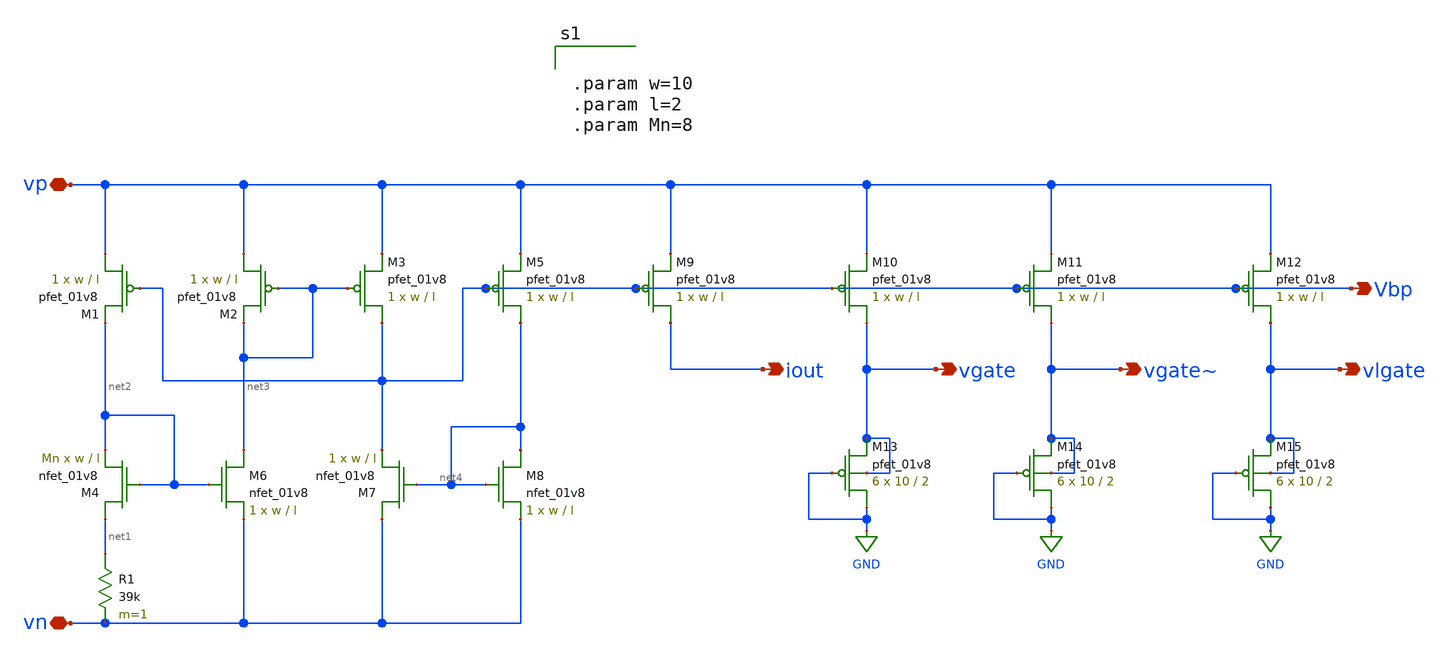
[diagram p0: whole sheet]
** sch_path: schematic/bias_current_resistive.sch
**.subckt bias_current_resistive vp vn iout vgate vgate~ Vbp vlgate
*.iopin vp
*.iopin vn
*.opin iout
*.opin vgate
*.opin vgate~
*.opin Vbp
*.opin vlgate
XM1 vp Vbp net2 VDD sky130_fd_pr__pfet_01v8 L=l W=w nf=1 ad='int((nf+1)/2) * W/nf * 0.29' as='int((nf+2)/2) * W/nf * 0.29'
+ pd='2*int((nf+1)/2) * (W/nf + 0.29)' ps='2*int((nf+2)/2) * (W/nf + 0.29)' nrd='0.29 / W' nrs='0.29 / W'
+ sa=0 sb=0 sd=0 mult=1 m=1
XM2 vp net3 net3 VDD sky130_fd_pr__pfet_01v8 L=l W=w nf=1 ad='int((nf+1)/2) * W/nf * 0.29' as='int((nf+2)/2) * W/nf * 0.29'
+ pd='2*int((nf+1)/2) * (W/nf + 0.29)' ps='2*int((nf+2)/2) * (W/nf + 0.29)' nrd='0.29 / W' nrs='0.29 / W'
+ sa=0 sb=0 sd=0 mult=1 m=1
XM3 Vbp net3 vp VDD sky130_fd_pr__pfet_01v8 L=l W=w nf=1 ad='int((nf+1)/2) * W/nf * 0.29' as='int((nf+2)/2) * W/nf * 0.29'
+ pd='2*int((nf+1)/2) * (W/nf + 0.29)' ps='2*int((nf+2)/2) * (W/nf + 0.29)' nrd='0.29 / W' nrs='0.29 / W'
+ sa=0 sb=0 sd=0 mult=1 m=1
XM5 net4 Vbp vp VDD sky130_fd_pr__pfet_01v8 L=l W=w nf=1 ad='int((nf+1)/2) * W/nf * 0.29' as='int((nf+2)/2) * W/nf * 0.29'
+ pd='2*int((nf+1)/2) * (W/nf + 0.29)' ps='2*int((nf+2)/2) * (W/nf + 0.29)' nrd='0.29 / W' nrs='0.29 / W'
+ sa=0 sb=0 sd=0 mult=1 m=1
XM4 net1 net2 net2 GND sky130_fd_pr__nfet_01v8 L=l W=w nf=1 ad='int((nf+1)/2) * W/nf * 0.29' as='int((nf+2)/2) * W/nf * 0.29'
+ pd='2*int((nf+1)/2) * (W/nf + 0.29)' ps='2*int((nf+2)/2) * (W/nf + 0.29)' nrd='0.29 / W' nrs='0.29 / W'
+ sa=0 sb=0 sd=0 mult=Mn m=Mn
XM6 net3 net2 vn GND sky130_fd_pr__nfet_01v8 L=l W=w nf=1 ad='int((nf+1)/2) * W/nf * 0.29' as='int((nf+2)/2) * W/nf * 0.29'
+ pd='2*int((nf+1)/2) * (W/nf + 0.29)' ps='2*int((nf+2)/2) * (W/nf + 0.29)' nrd='0.29 / W' nrs='0.29 / W'
+ sa=0 sb=0 sd=0 mult=1 m=1
XM7 vn net4 Vbp GND sky130_fd_pr__nfet_01v8 L=l W=w nf=1 ad='int((nf+1)/2) * W/nf * 0.29' as='int((nf+2)/2) * W/nf * 0.29'
+ pd='2*int((nf+1)/2) * (W/nf + 0.29)' ps='2*int((nf+2)/2) * (W/nf + 0.29)' nrd='0.29 / W' nrs='0.29 / W'
+ sa=0 sb=0 sd=0 mult=1 m=1
XM8 net4 net4 vn GND sky130_fd_pr__nfet_01v8 L=l W=w nf=1 ad='int((nf+1)/2) * W/nf * 0.29' as='int((nf+2)/2) * W/nf * 0.29'
+ pd='2*int((nf+1)/2) * (W/nf + 0.29)' ps='2*int((nf+2)/2) * (W/nf + 0.29)' nrd='0.29 / W' nrs='0.29 / W'
+ sa=0 sb=0 sd=0 mult=1 m=1
R1 net1 vn 39k m=1
XM9 iout Vbp vp VDD sky130_fd_pr__pfet_01v8 L=l W=w nf=1 ad='int((nf+1)/2) * W/nf * 0.29' as='int((nf+2)/2) * W/nf * 0.29'
+ pd='2*int((nf+1)/2) * (W/nf + 0.29)' ps='2*int((nf+2)/2) * (W/nf + 0.29)' nrd='0.29 / W' nrs='0.29 / W'
+ sa=0 sb=0 sd=0 mult=1 m=1
XM10 vgate Vbp vp VDD sky130_fd_pr__pfet_01v8 L=l W=w nf=1 ad='int((nf+1)/2) * W/nf * 0.29' as='int((nf+2)/2) * W/nf * 0.29'
+ pd='2*int((nf+1)/2) * (W/nf + 0.29)' ps='2*int((nf+2)/2) * (W/nf + 0.29)' nrd='0.29 / W' nrs='0.29 / W'
+ sa=0 sb=0 sd=0 mult=1 m=1
XM11 vgate~ Vbp vp VDD sky130_fd_pr__pfet_01v8 L=l W=w nf=1 ad='int((nf+1)/2) * W/nf * 0.29' as='int((nf+2)/2) * W/nf * 0.29'
+ pd='2*int((nf+1)/2) * (W/nf + 0.29)' ps='2*int((nf+2)/2) * (W/nf + 0.29)' nrd='0.29 / W' nrs='0.29 / W'
+ sa=0 sb=0 sd=0 mult=1 m=1
XM12 vlgate Vbp vp VDD sky130_fd_pr__pfet_01v8 L=l W=w nf=1 ad='int((nf+1)/2) * W/nf * 0.29' as='int((nf+2)/2) * W/nf * 0.29'
+ pd='2*int((nf+1)/2) * (W/nf + 0.29)' ps='2*int((nf+2)/2) * (W/nf + 0.29)' nrd='0.29 / W' nrs='0.29 / W'
+ sa=0 sb=0 sd=0 mult=1 m=1
XM13 GND GND vgate vgate sky130_fd_pr__pfet_01v8 L=2 W=10 nf=1 ad='int((nf+1)/2) * W/nf * 0.29' as='int((nf+2)/2) * W/nf * 0.29'
+ pd='2*int((nf+1)/2) * (W/nf + 0.29)' ps='2*int((nf+2)/2) * (W/nf + 0.29)' nrd='0.29 / W' nrs='0.29 / W'
+ sa=0 sb=0 sd=0 mult=6 m=6
XM14 GND GND vgate~ vgate~ sky130_fd_pr__pfet_01v8 L=2 W=10 nf=1 ad='int((nf+1)/2) * W/nf * 0.29' as='int((nf+2)/2) * W/nf * 0.29'
+ pd='2*int((nf+1)/2) * (W/nf + 0.29)' ps='2*int((nf+2)/2) * (W/nf + 0.29)' nrd='0.29 / W' nrs='0.29 / W'
+ sa=0 sb=0 sd=0 mult=6 m=6
XM15 GND GND vlgate vlgate sky130_fd_pr__pfet_01v8 L=2 W=10 nf=1 ad='int((nf+1)/2) * W/nf * 0.29' as='int((nf+2)/2) * W/nf * 0.29'
+ pd='2*int((nf+1)/2) * (W/nf + 0.29)' ps='2*int((nf+2)/2) * (W/nf + 0.29)' nrd='0.29 / W' nrs='0.29 / W'
+ sa=0 sb=0 sd=0 mult=6 m=6
**** begin user architecture code


.param w=10
.param l=2
.param Mn=8


**** end user architecture code
**.ends
.GLOBAL GND
.end
